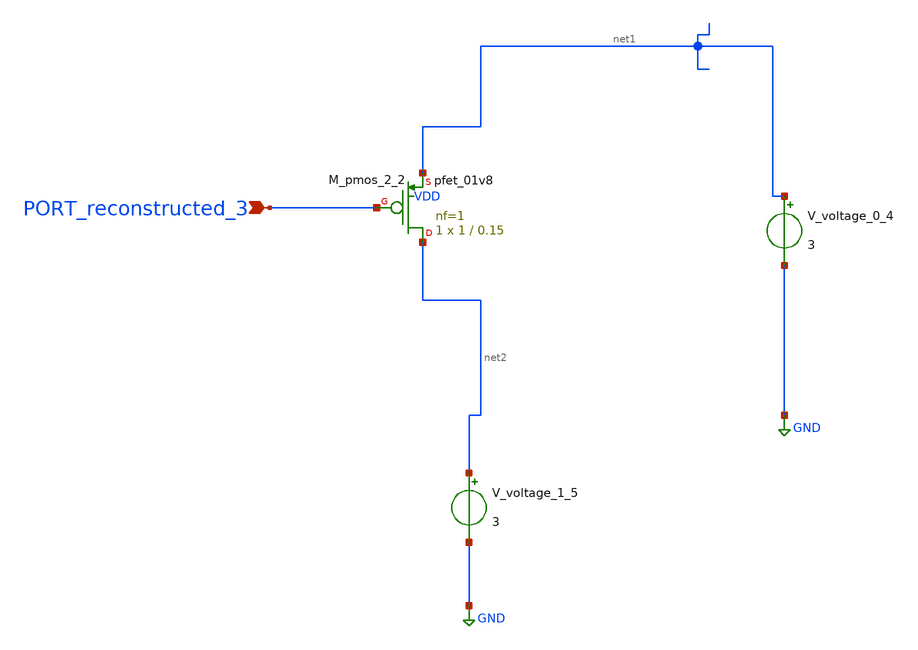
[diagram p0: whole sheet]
** sch_path: schematics/AMSNet/27.sch
**.subckt 27 PORT_reconstructed_3
*.ipin PORT_reconstructed_3
XM_pmos_2_2 net2 PORT_reconstructed_3 net1 VDD sky130_fd_pr__pfet_01v8 L=0.15 W=1 nf=1 ad='int((1 + 1)/2) * 1 / 1 * 0.29'
+ as='int((1 + 2)/2) * 1 / 1 * 0.29' pd='2*int((1 + 1)/2) * (1 / 1 + 0.29)' ps='2*int((1 + 2)/2) * (1 / 1 + 0.29)'
+ nrd='0.29 / 1 ' nrs='0.29 / 1 ' sa=0 sb=0 sd=0 mult=1 m=1
V_voltage_0_4 net1 GND 3
V_voltage_1_5 net2 GND 3
**.ends
.GLOBAL GND
.end
